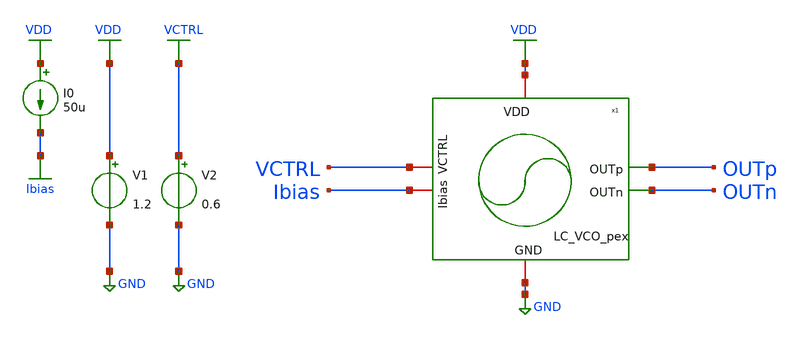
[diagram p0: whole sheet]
** sch_path: xschem/lc-vco/LC_VCO_pex_tb.sch
**.subckt LC_VCO_pex_tb
V1 VDD GND 1.2
V2 VCTRL GND 0.6
I0 VDD Ibias 50u
x1 VDD OUTp OUTn Ibias VCTRL GND LC_VCO_pex
**** begin user architecture code



.include ../simulations/LC_VCO.pex.spice
.include ./IHP_4nH_Inductor.spice
xind OUTp OUTn IHP_4nH_Inductor

.param temp = 27

.control

* Initial condition
.ic v(OUTp)=0.6

* Simulation accuracy
.options reltol=1e-4 abstol=1e-9 maxstep=5p method=gear

* Save required signals
save time v(OUTp) v(CTRL)

* Long transient for ~10 kHz FFT resolution
tran 0.01n 0.5u UIC

* Save raw waveform
write LC_VCO_tb.raw

* Plot steady-state waveform
plot v(OUTp) xlimit 5n 60n

* FFT analysis
linearize v(OUTp)
fft v(OUTp)

let vmag = db(mag(v(OUTp)))

* Plot FFT spectrum
plot vmag vs frequency xlimit 0 5G

* Save FFT data
wrdata fft_output.txt frequency vmag

* Save waveform for external processing
wrdata vco_waveform.txt time v(OUTp)

.endc



 .lib cornerMOSlv.lib mos_tt
.lib cornerRES.lib res_typ
.lib $::SG13G2_MODELS/cornerCAP.lib cap_typ_stat

**** end user architecture code
**.ends
.GLOBAL GND
.GLOBAL VDD
.GLOBAL VCTRL
.GLOBAL Ibias
.end
